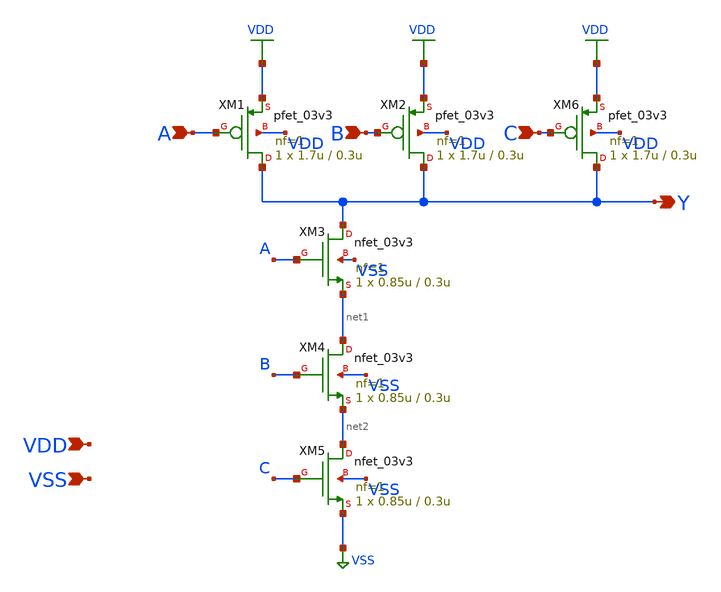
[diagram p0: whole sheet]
** sch_path: designs/comparator/final_magic/nand3/nand3_1.sch
**.subckt nand3_1 A B Y VDD VSS C
*.ipin A
*.ipin B
*.opin Y
*.ipin VDD
*.ipin VSS
*.ipin C
XM1 Y A VDD VDD pfet_03v3 L=0.3u W=1.7u nf=1 ad='int((nf+1)/2) * W/nf * 0.18u' as='int((nf+2)/2) * W/nf * 0.18u'
+ pd='2*int((nf+1)/2) * (W/nf + 0.18u)' ps='2*int((nf+2)/2) * (W/nf + 0.18u)' nrd='0.18u / W' nrs='0.18u / W'
+ sa=0 sb=0 sd=0 m=1
XM2 Y B VDD VDD pfet_03v3 L=0.3u W=1.7u nf=1 ad='int((nf+1)/2) * W/nf * 0.18u' as='int((nf+2)/2) * W/nf * 0.18u'
+ pd='2*int((nf+1)/2) * (W/nf + 0.18u)' ps='2*int((nf+2)/2) * (W/nf + 0.18u)' nrd='0.18u / W' nrs='0.18u / W'
+ sa=0 sb=0 sd=0 m=1
XM3 Y A net1 VSS nfet_03v3 L=0.3u W=0.85u nf=1 ad='int((nf+1)/2) * W/nf * 0.18u' as='int((nf+2)/2) * W/nf * 0.18u'
+ pd='2*int((nf+1)/2) * (W/nf + 0.18u)' ps='2*int((nf+2)/2) * (W/nf + 0.18u)' nrd='0.18u / W' nrs='0.18u / W'
+ sa=0 sb=0 sd=0 m=1
XM4 net1 B net2 VSS nfet_03v3 L=0.3u W=0.85u nf=1 ad='int((nf+1)/2) * W/nf * 0.18u' as='int((nf+2)/2) * W/nf * 0.18u'
+ pd='2*int((nf+1)/2) * (W/nf + 0.18u)' ps='2*int((nf+2)/2) * (W/nf + 0.18u)' nrd='0.18u / W' nrs='0.18u / W'
+ sa=0 sb=0 sd=0 m=1
XM5 net2 C VSS VSS nfet_03v3 L=0.3u W=0.85u nf=1 ad='int((nf+1)/2) * W/nf * 0.18u' as='int((nf+2)/2) * W/nf * 0.18u'
+ pd='2*int((nf+1)/2) * (W/nf + 0.18u)' ps='2*int((nf+2)/2) * (W/nf + 0.18u)' nrd='0.18u / W' nrs='0.18u / W'
+ sa=0 sb=0 sd=0 m=1
XM6 Y C VDD VDD pfet_03v3 L=0.3u W=1.7u nf=1 ad='int((nf+1)/2) * W/nf * 0.18u' as='int((nf+2)/2) * W/nf * 0.18u'
+ pd='2*int((nf+1)/2) * (W/nf + 0.18u)' ps='2*int((nf+2)/2) * (W/nf + 0.18u)' nrd='0.18u / W' nrs='0.18u / W'
+ sa=0 sb=0 sd=0 m=1
**.ends
.GLOBAL VDD
.GLOBAL VSS
.end
